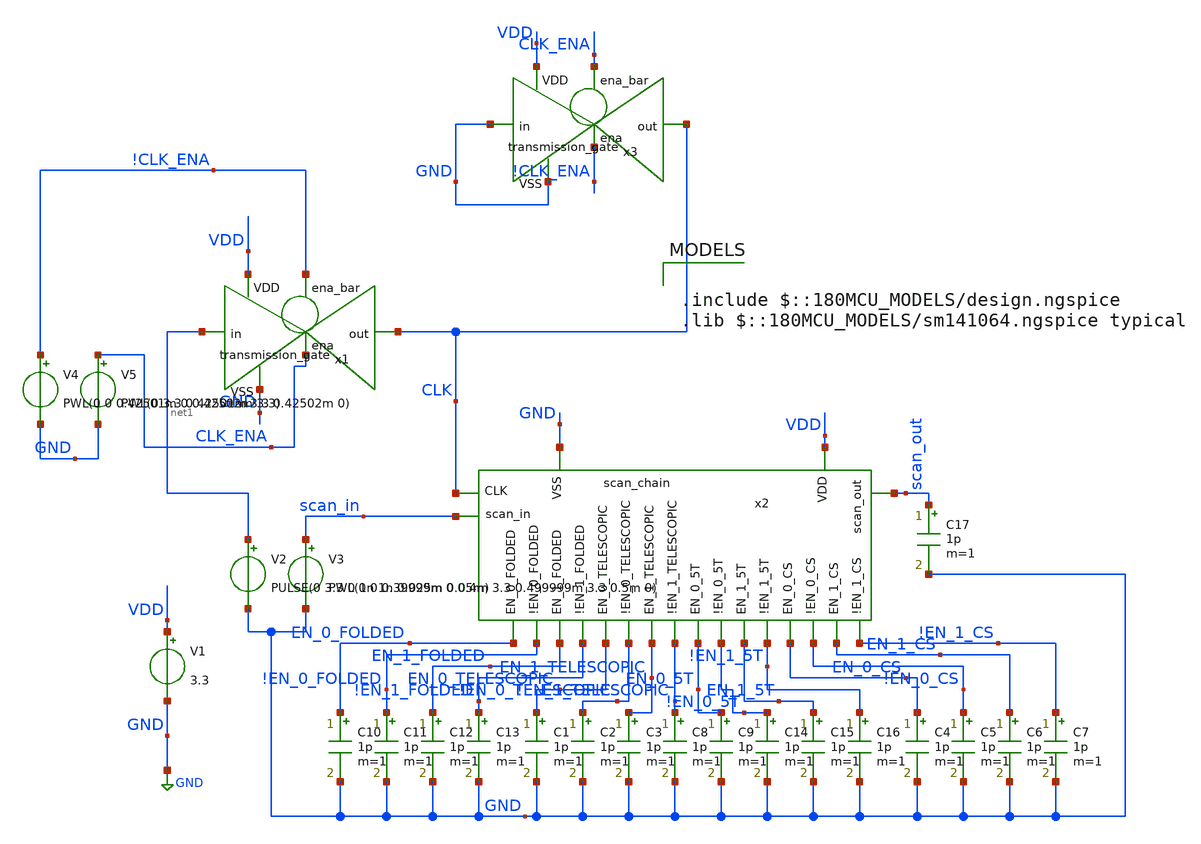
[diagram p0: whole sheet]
** sch_path: designs/libs/core_digital/tb/TB_scan_chain.sch
**.subckt TB_scan_chain
V1 VDD GND 3.3
C1 EN_0_TELESCOPIC GND 1p m=1
C2 !EN_0_TELESCOPIC GND 1p m=1
C3 EN_1_TELESCOPIC GND 1p m=1
C8 !EN_1_TELESCOPIC GND 1p m=1
C10 EN_0_FOLDED GND 1p m=1
C11 !EN_0_FOLDED GND 1p m=1
C12 EN_1_FOLDED GND 1p m=1
C13 !EN_1_FOLDED GND 1p m=1
C4 EN_0_CS GND 1p m=1
C5 !EN_0_CS GND 1p m=1
C6 EN_1_CS GND 1p m=1
C7 !EN_1_CS GND 1p m=1
C9 EN_0_5T GND 1p m=1
C14 !EN_0_5T GND 1p m=1
C15 EN_1_5T GND 1p m=1
C16 !EN_1_5T GND 1p m=1
C17 scan_out GND 1p m=1
V2 net1 GND PULSE(0 3.3 0 1n 1n 0.025m 0.05m)
V3 scan_in GND PWL(0 0 0.39999m 0 0.4m 3.3 0.499999m 3.3 0.5m 0)
x2 VDD scan_out EN_1_5T EN_0_5T EN_0_CS EN_1_CS EN_0_TELESCOPIC EN_1_FOLDED EN_0_FOLDED
+ EN_1_TELESCOPIC scan_in !EN_1_FOLDED !EN_1_CS !EN_0_TELESCOPIC !EN_0_CS !EN_1_5T !EN_0_5T !EN_1_TELESCOPIC
+ !EN_0_FOLDED CLK GND scan_chain
x1 !CLK_ENA VDD CLK net1 GND CLK_ENA transmission_gate
V4 !CLK_ENA GND PWL(0 0 0.42501m 0 0.42502m 3.3)
V5 CLK_ENA GND PWL(0 3.3 0.42501m 3.3 0.42502m 0)
x3 CLK_ENA VDD CLK GND GND !CLK_ENA transmission_gate
**** begin user architecture code

.include $::180MCU_MODELS/design.ngspice
.lib $::180MCU_MODELS/sm141064.ngspice typical

 * Transient Analysis - 10ms
.tran 1u 20m

* NGSpice interactive plot command
.control
  run
  plot V(scan_in) title 'Scan In' xlabel 'Time (s)' ylabel 'Voltage (V)'
  plot V(CLK)
  plot V(EN_0_FOLDED) V(!EN_0_FOLDED) title 'Folded Enable 0' xlabel 'Time (s)' ylabel 'Voltage (V)'
  *plot V(EN_1_FOLDED) V(!EN_1_FOLDED) title 'Folded Enable 1' xlabel 'Time (s)' ylabel 'Voltage (V)'
  *plot V(EN_0_TELESCOPIC) V(!EN_0_TELESCOPIC) title 'Telescopic Enable 0' xlabel 'Time (s)' ylabel 'Voltage (V)'
 * plot V(EN_1_TELESCOPIC) V(!EN_1_TELESCOPIC) title 'Telescopic Enable 1' xlabel 'Time (s)' ylabel 'Voltage (V)'
  *plot V(EN_0_5T) V(!EN_0_5T) title '5T Enable 0' xlabel 'Time (s)' ylabel 'Voltage (V)'
 * plot V(EN_1_5T) V(!EN_1_5T) title '5T Enable 1' xlabel 'Time (s)' ylabel 'Voltage (V)'
 * plot V(EN_0_CS) V(!EN_0_CS) title 'CS Enable 0' xlabel 'Time (s)' ylabel 'Voltage (V)'
 * plot V(EN_1_CS) V(!EN_1_CS) title 'CS Enable 1' xlabel 'Time (s)' ylabel 'Voltage (V)'
.endc

.end
**** end user architecture code
**.ends
.GLOBAL GND
.end
